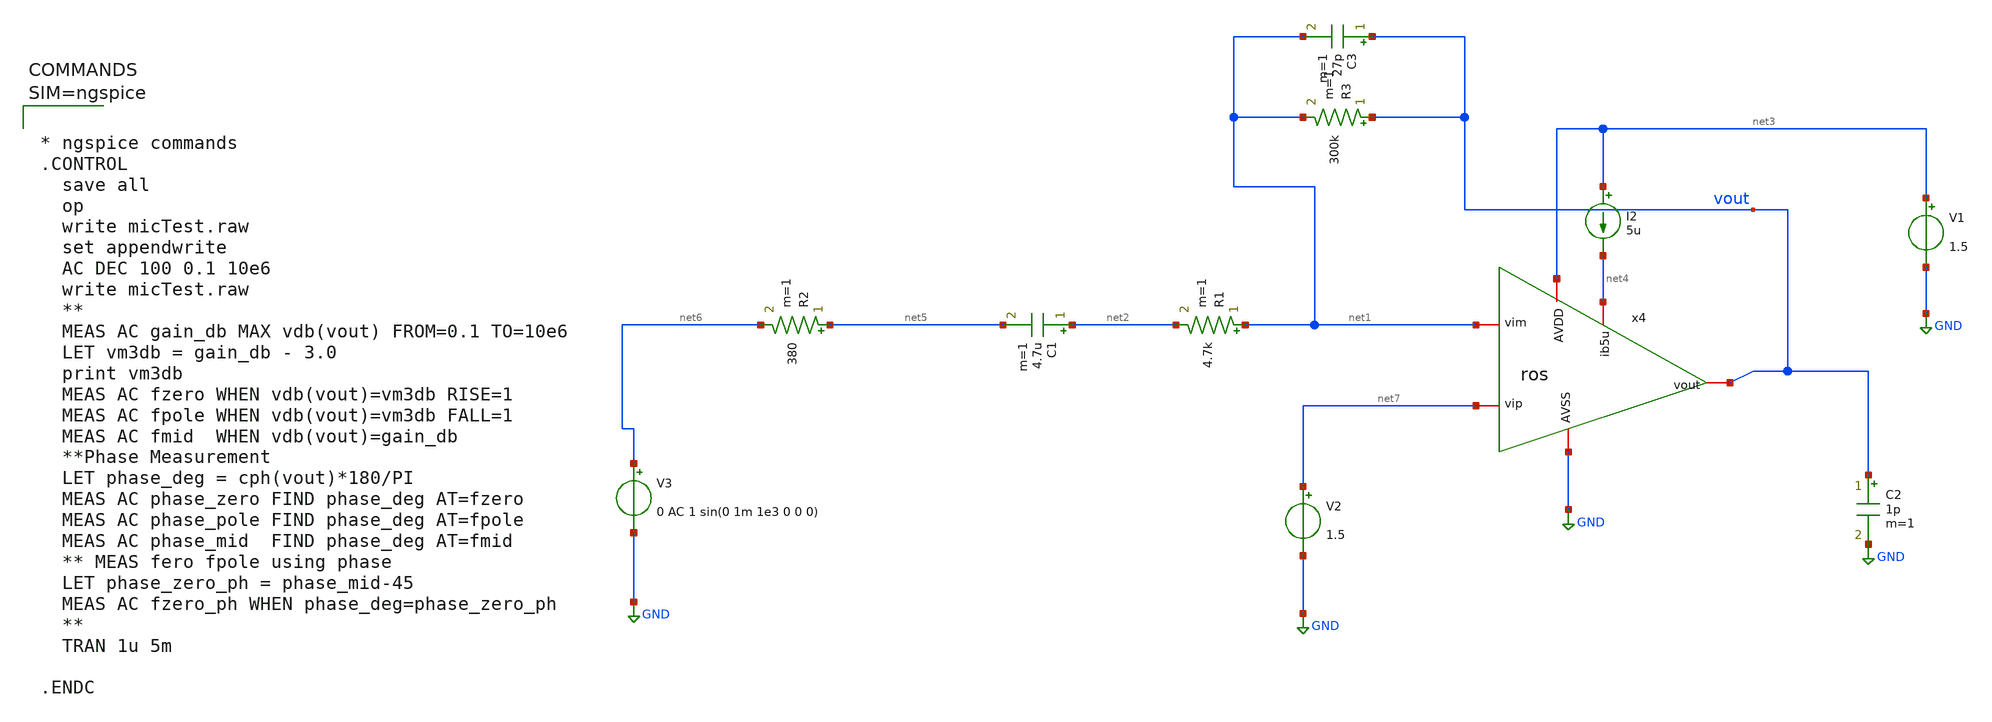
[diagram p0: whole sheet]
** sch_path: xschem/united.sch
**.subckt united
x4 net3 vout net7 net1 net4 GND ros
R1 net1 net2 4.7k m=1
C1 net2 net5 4.7u m=1
R2 net5 net6 380 m=1
C2 vout GND 1p m=1
I2 net3 net4 5u
V1 net3 GND 1.5
C3 vout net1 27p m=1
R3 vout net1 300k m=1
V2 net7 GND 1.5
V3 net6 GND 0 AC 1 sin(0 1m 1e3 0 0 0)
**** begin user architecture code



* ngspice commands
.CONTROL
  save all
  op
  write micTest.raw
  set appendwrite
  AC DEC 100 0.1 10e6
  write micTest.raw
  **
  MEAS AC gain_db MAX vdb(vout) FROM=0.1 TO=10e6
  LET vm3db = gain_db - 3.0
  print vm3db
  MEAS AC fzero WHEN vdb(vout)=vm3db RISE=1
  MEAS AC fpole WHEN vdb(vout)=vm3db FALL=1
  MEAS AC fmid  WHEN vdb(vout)=gain_db
  **Phase Measurement
  LET phase_deg = cph(vout)*180/PI
  MEAS AC phase_zero FIND phase_deg AT=fzero
  MEAS AC phase_pole FIND phase_deg AT=fpole
  MEAS AC phase_mid  FIND phase_deg AT=fmid
  ** MEAS fero fpole using phase
  LET phase_zero_ph = phase_mid-45
  MEAS AC fzero_ph WHEN phase_deg=phase_zero_ph
  **
  TRAN 1u 5m

.ENDC



**** end user architecture code
**.ends

* expanding   symbol:  ros.sym # of pins=6
** sym_path: xschem/ros.sym
** sch_path: xschem/ros.sch
.subckt ros AVDD vout vip vim ib5u AVSS
*.iopin vip
*.iopin AVSS
*.iopin AVDD
*.iopin ib5u
*.iopin vim
*.iopin vout
XM10 AVDD net1 net2 AVDD sky130_fd_pr__pfet_01v8_lvt L=0.35 W=1 nf=1 ad='int((1 + 1)/2) * 1 / 1 * 0.29'
+ as='int((1 + 2)/2) * 1 / 1 * 0.29' pd='2*int((1 + 1)/2) * (1 / 1 + 0.29)' ps='2*int((1 + 2)/2) * (1 / 1 + 0.29)'
+ nrd='0.29 / 1 ' nrs='0.29 / 1 ' sa=0 sb=0 sd=0 mult=1 m=1
XM1 vout net1 AVDD AVDD sky130_fd_pr__pfet_01v8_lvt L=0.35 W=1 nf=1 ad='int((1 + 1)/2) * 1 / 1 * 0.29'
+ as='int((1 + 2)/2) * 1 / 1 * 0.29' pd='2*int((1 + 1)/2) * (1 / 1 + 0.29)' ps='2*int((1 + 2)/2) * (1 / 1 + 0.29)'
+ nrd='0.29 / 1 ' nrs='0.29 / 1 ' sa=0 sb=0 sd=0 mult=1 m=1
XM2 net2 vip net3 net3 sky130_fd_pr__nfet_01v8_lvt L=2 W=4 nf=1 ad='int((1 + 1)/2) * 4 / 1 * 0.29' as='int((1 + 2)/2) * 4 / 1 * 0.29'
+ pd='2*int((1 + 1)/2) * (4 / 1 + 0.29)' ps='2*int((1 + 2)/2) * (4 / 1 + 0.29)' nrd='0.29 / 4 ' nrs='0.29 / 4 '
+ sa=0 sb=0 sd=0 mult=5 m=5
XM3 net3 vim vout net3 sky130_fd_pr__nfet_01v8_lvt L=0.15 W=1 nf=1 ad='int((1 + 1)/2) * 1 / 1 * 0.29'
+ as='int((1 + 2)/2) * 1 / 1 * 0.29' pd='2*int((1 + 1)/2) * (1 / 1 + 0.29)' ps='2*int((1 + 2)/2) * (1 / 1 + 0.29)'
+ nrd='0.29 / 1 ' nrs='0.29 / 1 ' sa=0 sb=0 sd=0 mult=1 m=1
XM4 AVSS ib5u ib5u AVSS sky130_fd_pr__nfet_01v8 L=0.15 W=1 nf=1 ad='int((1 + 1)/2) * 1 / 1 * 0.29' as='int((1 + 2)/2) * 1 / 1 * 0.29'
+ pd='2*int((1 + 1)/2) * (1 / 1 + 0.29)' ps='2*int((1 + 2)/2) * (1 / 1 + 0.29)' nrd='0.29 / 1 ' nrs='0.29 / 1 '
+ sa=0 sb=0 sd=0 mult=1 m=1
XM5 net3 ib5u AVSS AVSS sky130_fd_pr__nfet_01v8 L=0.15 W=1 nf=1 ad='int((1 + 1)/2) * 1 / 1 * 0.29' as='int((1 + 2)/2) * 1 / 1 * 0.29'
+ pd='2*int((1 + 1)/2) * (1 / 1 + 0.29)' ps='2*int((1 + 2)/2) * (1 / 1 + 0.29)' nrd='0.29 / 1 ' nrs='0.29 / 1 '
+ sa=0 sb=0 sd=0 mult=1 m=1
.ends

.GLOBAL GND
.end
